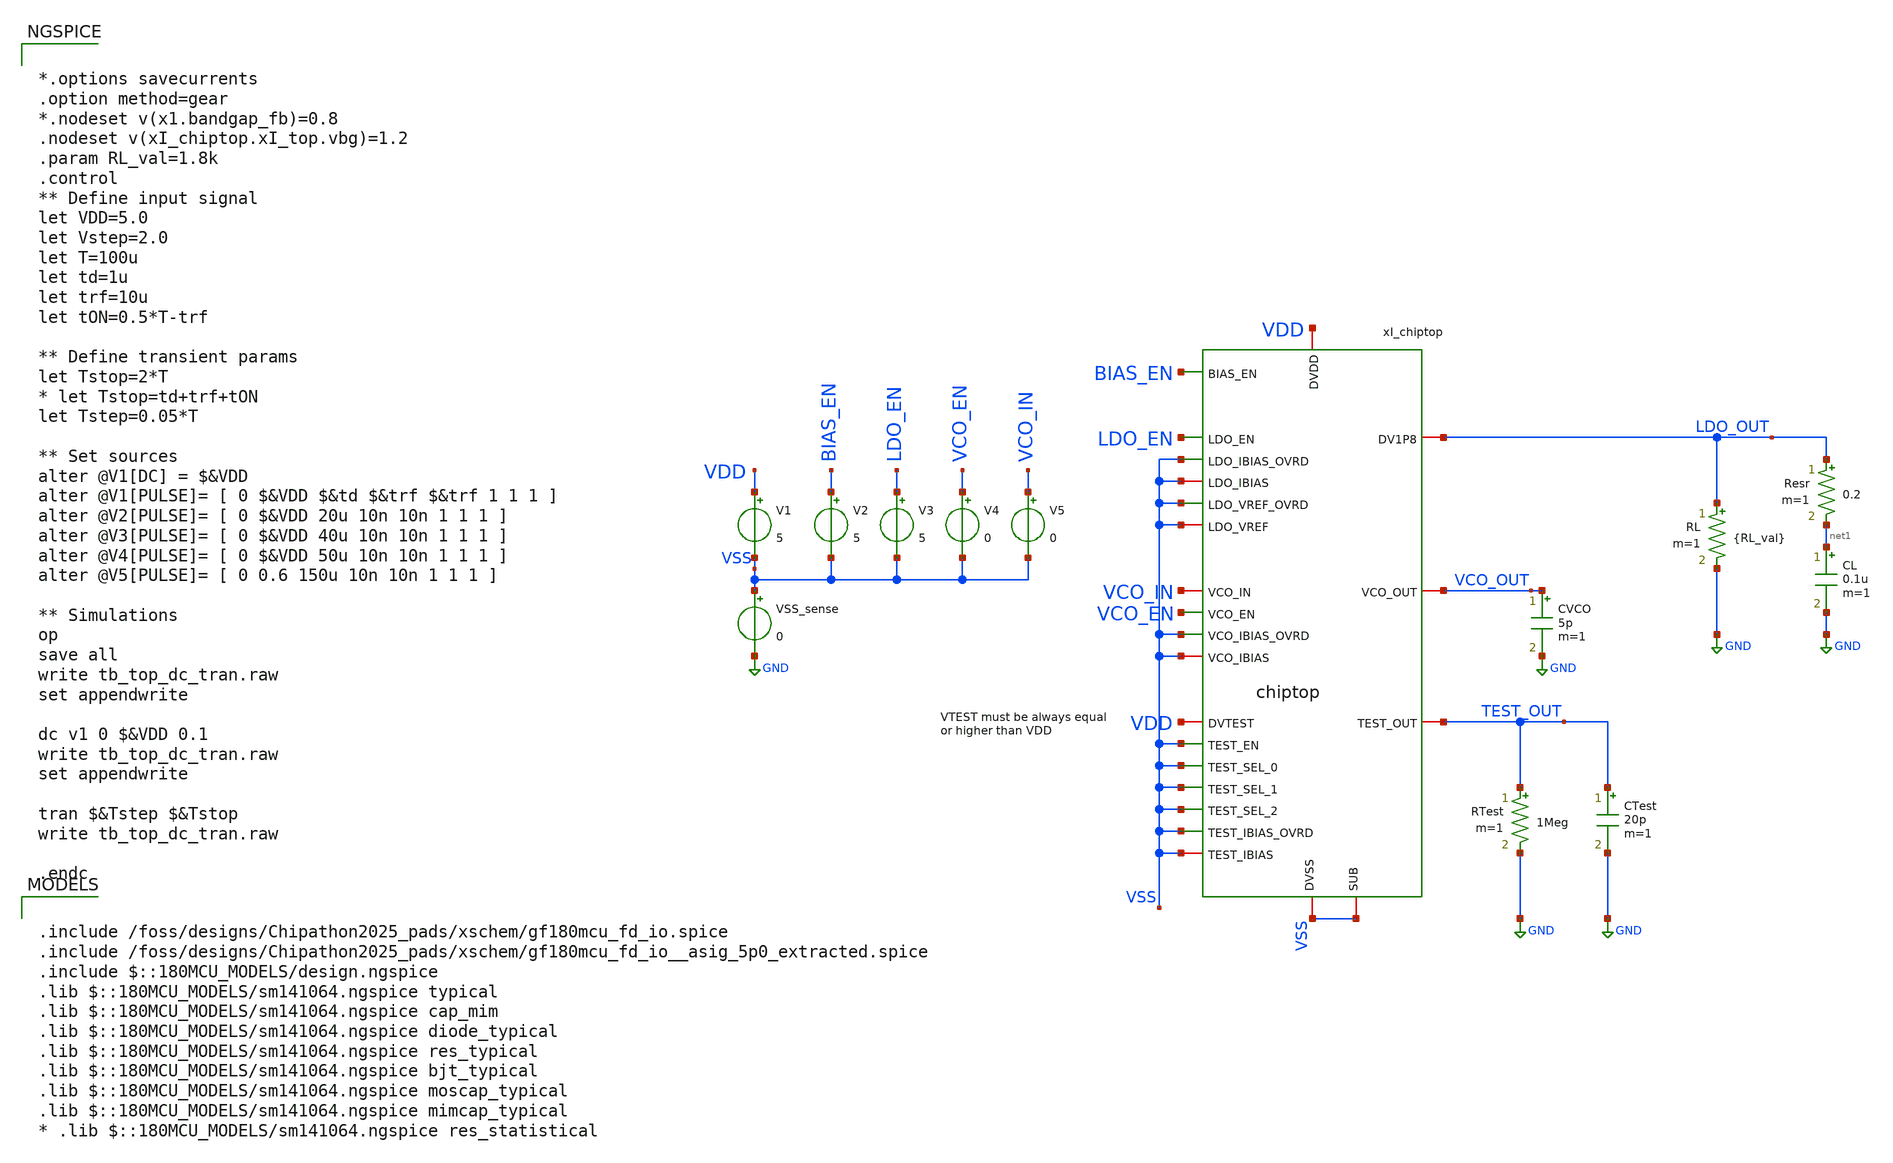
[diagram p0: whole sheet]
** sch_path: designs/libs/tb_top/tb_chiptop_dc_tran/tb_chiptop_dc_tran.sch
**.subckt tb_chiptop_dc_tran
V1 VDD VSS 5
VSS_sense VSS GND 0
V2 BIAS_EN VSS 5
V3 LDO_EN VSS 5
V4 VCO_EN VSS 0
V5 VCO_IN VSS 0
RL LDO_OUT GND {RL_val} m=1
CL net1 GND 0.1u m=1
Resr LDO_OUT net1 0.2 m=1
RTest TEST_OUT GND 1Meg m=1
CTest TEST_OUT GND 20p m=1
CVCO VCO_OUT GND 5p m=1
xI_chiptop VDD LDO_OUT VDD VSS VCO_IN VCO_EN TEST_OUT VSS VSS VSS VSS VSS VSS VSS LDO_EN VSS VSS VSS
+ VSS VSS VSS BIAS_EN VCO_OUT chiptop
**** begin user architecture code

.include /foss/designs/Chipathon2025_pads/xschem/gf180mcu_fd_io.spice
.include /foss/designs/Chipathon2025_pads/xschem/gf180mcu_fd_io__asig_5p0_extracted.spice
.include $::180MCU_MODELS/design.ngspice
.lib $::180MCU_MODELS/sm141064.ngspice typical
.lib $::180MCU_MODELS/sm141064.ngspice cap_mim
.lib $::180MCU_MODELS/sm141064.ngspice diode_typical
.lib $::180MCU_MODELS/sm141064.ngspice res_typical
.lib $::180MCU_MODELS/sm141064.ngspice bjt_typical
.lib $::180MCU_MODELS/sm141064.ngspice moscap_typical
.lib $::180MCU_MODELS/sm141064.ngspice mimcap_typical
* .lib $::180MCU_MODELS/sm141064.ngspice res_statistical



*.options savecurrents
.option method=gear
*.nodeset v(x1.bandgap_fb)=0.8
.nodeset v(xI_chiptop.xI_top.vbg)=1.2
.param RL_val=1.8k
.control
** Define input signal
let VDD=5.0
let Vstep=2.0
let T=100u
let td=1u
let trf=10u
let tON=0.5*T-trf

** Define transient params
let Tstop=2*T
* let Tstop=td+trf+tON
let Tstep=0.05*T

** Set sources
alter @V1[DC] = $&VDD
alter @V1[PULSE]= [ 0 $&VDD $&td $&trf $&trf 1 1 1 ]
alter @V2[PULSE]= [ 0 $&VDD 20u 10n 10n 1 1 1 ]
alter @V3[PULSE]= [ 0 $&VDD 40u 10n 10n 1 1 1 ]
alter @V4[PULSE]= [ 0 $&VDD 50u 10n 10n 1 1 1 ]
alter @V5[PULSE]= [ 0 0.6 150u 10n 10n 1 1 1 ]

** Simulations
op
save all
write tb_top_dc_tran.raw
set appendwrite

dc v1 0 $&VDD 0.1
write tb_top_dc_tran.raw
set appendwrite

tran $&Tstep $&Tstop
write tb_top_dc_tran.raw

.endc


**** end user architecture code
**.ends
.GLOBAL GND
.end
